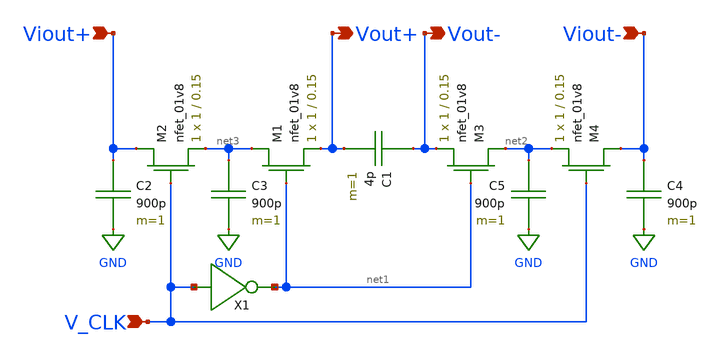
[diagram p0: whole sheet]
** sch_path: simulation/filter/filter_switch_cap.sch
**.subckt filter_switch_cap Viout+ Viout- Vout+ Vout- V_CLK
*.ipin Viout+
*.ipin Viout-
*.opin Vout+
*.opin Vout-
*.ipin V_CLK
C1 Vout- Vout+ 4p m=1
C3 net3 GND 900p m=1
XM1 net3 net1 Vout+ GND sky130_fd_pr__nfet_01v8 L=0.15 W=1 nf=1 ad='int((nf+1)/2) * W/nf * 0.29' as='int((nf+2)/2) * W/nf * 0.29'
+ pd='2*int((nf+1)/2) * (W/nf + 0.29)' ps='2*int((nf+2)/2) * (W/nf + 0.29)' nrd='0.29 / W' nrs='0.29 / W'
+ sa=0 sb=0 sd=0 mult=1 m=1
XM2 Viout+ V_CLK net3 GND sky130_fd_pr__nfet_01v8 L=0.15 W=1 nf=1 ad='int((nf+1)/2) * W/nf * 0.29' as='int((nf+2)/2) * W/nf * 0.29'
+ pd='2*int((nf+1)/2) * (W/nf + 0.29)' ps='2*int((nf+2)/2) * (W/nf + 0.29)' nrd='0.29 / W' nrs='0.29 / W'
+ sa=0 sb=0 sd=0 mult=1 m=1
X1 V_CLK net1 inverter
C5 net2 GND 900p m=1
XM3 net2 net1 Vout- GND sky130_fd_pr__nfet_01v8 L=0.15 W=1 nf=1 ad='int((nf+1)/2) * W/nf * 0.29' as='int((nf+2)/2) * W/nf * 0.29'
+ pd='2*int((nf+1)/2) * (W/nf + 0.29)' ps='2*int((nf+2)/2) * (W/nf + 0.29)' nrd='0.29 / W' nrs='0.29 / W'
+ sa=0 sb=0 sd=0 mult=1 m=1
XM4 Viout- V_CLK net2 GND sky130_fd_pr__nfet_01v8 L=0.15 W=1 nf=1 ad='int((nf+1)/2) * W/nf * 0.29' as='int((nf+2)/2) * W/nf * 0.29'
+ pd='2*int((nf+1)/2) * (W/nf + 0.29)' ps='2*int((nf+2)/2) * (W/nf + 0.29)' nrd='0.29 / W' nrs='0.29 / W'
+ sa=0 sb=0 sd=0 mult=1 m=1
C2 Viout+ GND 900p m=1
C4 Viout- GND 900p m=1
**.ends

* expanding   symbol:  /home/madvlsi/VLSI_Sine_Gen/simulation/dac/inverter.sym # of pins=2
** sym_path: simulation/dac/inverter.sym
** sch_path: simulation/dac/inverter.sch
.subckt inverter A Y
*.ipin A
*.opin Y
XM1 Y A VDD VDD sky130_fd_pr__pfet_01v8 L=0.15 W=1 nf=1 ad='int((nf+1)/2) * W/nf * 0.29' as='int((nf+2)/2) * W/nf * 0.29'
+ pd='2*int((nf+1)/2) * (W/nf + 0.29)' ps='2*int((nf+2)/2) * (W/nf + 0.29)' nrd='0.29 / W' nrs='0.29 / W'
+ sa=0 sb=0 sd=0 mult=1 m=1
XM2 Y A GND GND sky130_fd_pr__nfet_01v8 L=0.15 W=1 nf=1 ad='int((nf+1)/2) * W/nf * 0.29' as='int((nf+2)/2) * W/nf * 0.29'
+ pd='2*int((nf+1)/2) * (W/nf + 0.29)' ps='2*int((nf+2)/2) * (W/nf + 0.29)' nrd='0.29 / W' nrs='0.29 / W'
+ sa=0 sb=0 sd=0 mult=1 m=1
.ends

.GLOBAL GND
.GLOBAL VDD
.end
